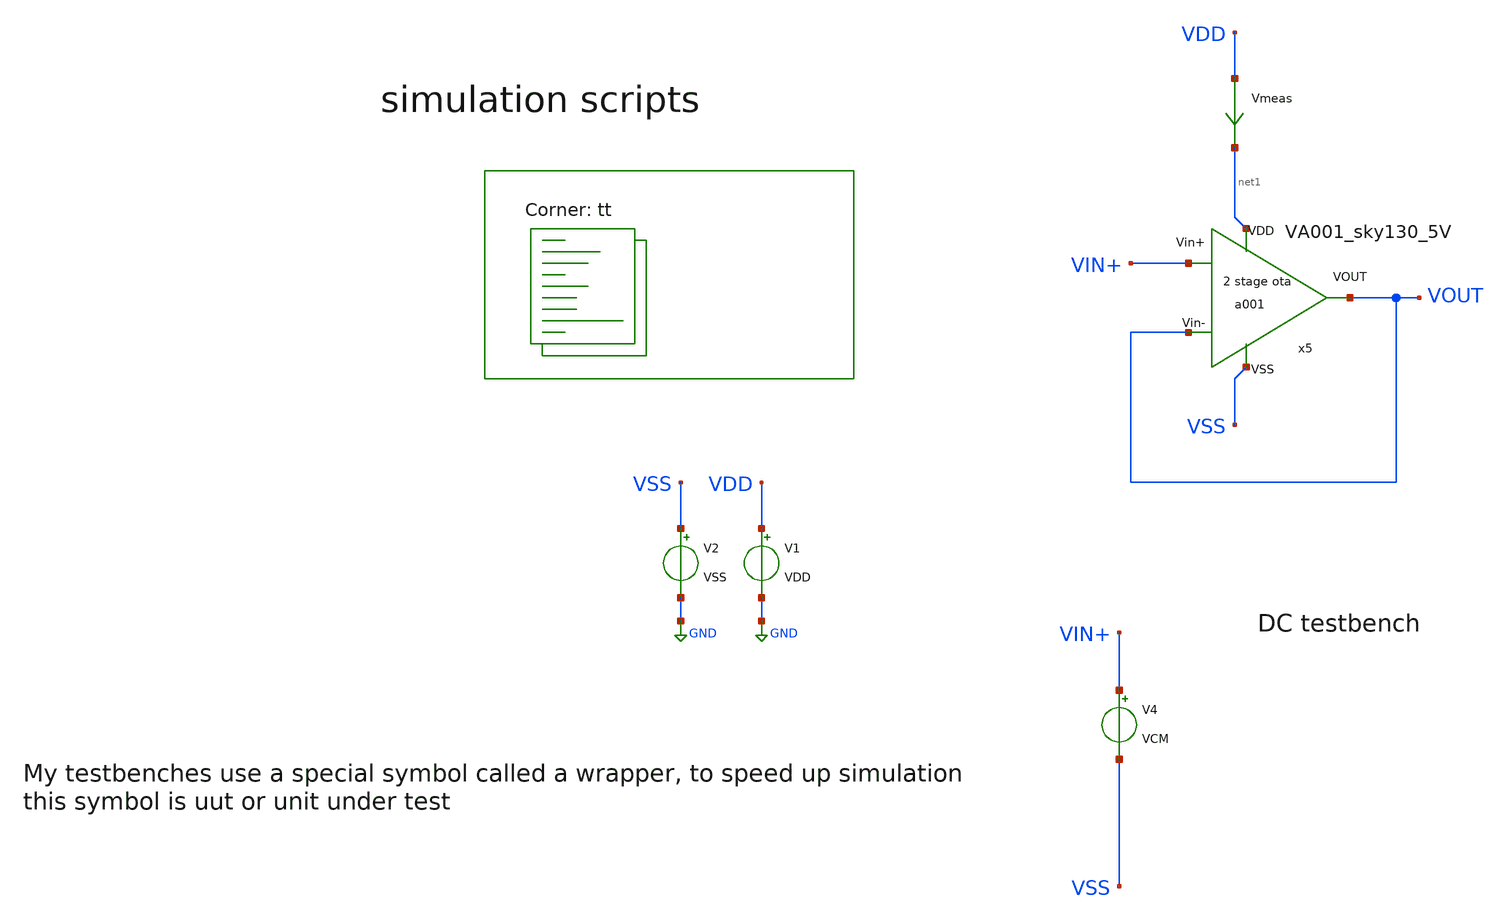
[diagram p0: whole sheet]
** sch_path: Learning/single_ended_amplifiers/Design_and_Analysis_of_Two-Stage_CMOS_Operational_Amplifier_for_Fluorescence_Signal_Processing_sky130_5V/amplifier_design/OTA_DC_TB.sch
**.subckt OTA_DC_TB
V1 VDD GND VDD
V2 VSS GND VSS
V4 VIN+ VSS VCM
Vmeas VDD net1 0
.save i(vmeas)
x5 net1 VSS VIN+ VOUT VOUT VA001_sky130_5V
**** begin user architecture code
.lib $::SKYWATER_MODELS/sky130.lib.spice tt

.Temp 27
.param VDD = 5
.param VSS = 0
.param VCM = 2.5


.control
save all
dc V4 0 5 0.01
wrdata VIN_sweep_DC.csv v(VOUT) i(Vmeas)
plot v(VOUT) v(VIN+)
plot i(Vmeas)
op
.endc


**** end user architecture code
**.ends

* expanding   symbol:  Sky130A/single ended amplifiers/VA001_sky130_5V.sym # of pins=5
** sym_path: LIB/Sky130A/single ended amplifiers/VA001_sky130_5V.sym
** sch_path: LIB/Sky130A/single ended amplifiers/VA001_sky130_5V.sch
.subckt VA001_sky130_5V VDD VSS Vin+ Vin- VOUT
*.iopin VDD
*.iopin VSS
*.iopin Vin+
*.iopin Vin-
*.iopin VOUT
XM9 VB1 VB2 net3 VSS sky130_fd_pr__nfet_g5v0d10v5 L=2 W='1 * 2 ' nf=2 ad='int((nf+1)/2) * W / nf * 0.29'
+ as='int((nf+2)/2) * W / nf * 0.29' pd='2*int((nf+1)/2) * (W / nf + 0.29)' ps='2*int((nf+2)/2) * (W / nf + 0.29)'
+ nrd='0.29 / W ' nrs='0.29 / W ' sa=0 sb=0 sd=0 mult=2 m=2
XM10 VB2 VB2 net1 VSS sky130_fd_pr__nfet_g5v0d10v5 L=2 W='1 * 2 ' nf=2 ad='int((nf+1)/2) * W / nf * 0.29'
+ as='int((nf+2)/2) * W / nf * 0.29' pd='2*int((nf+1)/2) * (W / nf + 0.29)' ps='2*int((nf+2)/2) * (W / nf + 0.29)'
+ nrd='0.29 / W ' nrs='0.29 / W ' sa=0 sb=0 sd=0 mult=2 m=2
XM3 VB2 VB1 VDD VDD sky130_fd_pr__pfet_g5v0d10v5 L=2.5 W='1 * 2 ' nf=2 ad='int((2 + 1)/2) * 1 * 0.29'
+ as='int((2 + 2)/2) * 1 * 0.29' pd='2*int((2 + 1)/2) * (1 + 0.29)' ps='2*int((2 + 2)/2) * (1 + 0.29)'
+ nrd='0.29 / 1 / 2 ' nrs='0.29 / 1 / 2 ' sa=0 sb=0 sd=0 mult=2 m=2
XM4 VB1 VB1 VDD VDD sky130_fd_pr__pfet_g5v0d10v5 L=2.5 W='1 * 2 ' nf=2 ad='int((2 + 1)/2) * 1 * 0.29'
+ as='int((2 + 2)/2) * 1 * 0.29' pd='2*int((2 + 1)/2) * (1 + 0.29)' ps='2*int((2 + 2)/2) * (1 + 0.29)'
+ nrd='0.29 / 1 / 2 ' nrs='0.29 / 1 / 2 ' sa=0 sb=0 sd=0 mult=2 m=2
XM5 net1 net1 VSS VSS sky130_fd_pr__nfet_g5v0d10v5 L=3 W='1.2 * 2 ' nf=2 ad='int((nf+1)/2) * W / nf * 0.29'
+ as='int((nf+2)/2) * W / nf * 0.29' pd='2*int((nf+1)/2) * (W / nf + 0.29)' ps='2*int((nf+2)/2) * (W / nf + 0.29)'
+ nrd='0.29 / W ' nrs='0.29 / W ' sa=0 sb=0 sd=0 mult=2 m=2
XM6 net3 net1 net2 VSS sky130_fd_pr__nfet_g5v0d10v5 L=3 W='1.2 * 2 ' nf=2 ad='int((nf+1)/2) * W / nf * 0.29'
+ as='int((nf+2)/2) * W / nf * 0.29' pd='2*int((nf+1)/2) * (W / nf + 0.29)' ps='2*int((nf+2)/2) * (W / nf + 0.29)'
+ nrd='0.29 / W ' nrs='0.29 / W ' sa=0 sb=0 sd=0 mult=8 m=8
XR2 VSS net2 VSS sky130_fd_pr__res_high_po_0p35 L=20 mult=1 m=1
XM1 net4 VB1 VDD VDD sky130_fd_pr__pfet_g5v0d10v5 L=2.5 W='1 * 2 ' nf=2 ad='int((2 + 1)/2) * 1 * 0.29'
+ as='int((2 + 2)/2) * 1 * 0.29' pd='2*int((2 + 1)/2) * (1 + 0.29)' ps='2*int((2 + 2)/2) * (1 + 0.29)'
+ nrd='0.29 / 1 / 2 ' nrs='0.29 / 1 / 2 ' sa=0 sb=0 sd=0 mult=6 m=6
XM2 net6 Vin- net4 net4 sky130_fd_pr__pfet_g5v0d10v5 L=1 W='3 * 2 ' nf=2 ad='int((2 + 1)/2) * 3 * 0.29'
+ as='int((2 + 2)/2) * 3 * 0.29' pd='2*int((2 + 1)/2) * (3 + 0.29)' ps='2*int((2 + 2)/2) * (3 + 0.29)'
+ nrd='0.29 / 3 / 2 ' nrs='0.29 / 3 / 2 ' sa=0 sb=0 sd=0 mult=4 m=4
XM11 net6 net6 VSS VSS sky130_fd_pr__nfet_g5v0d10v5 L=2 W='1.2 * 2 ' nf=2 ad='int((nf+1)/2) * W / nf * 0.29'
+ as='int((nf+2)/2) * W / nf * 0.29' pd='2*int((nf+1)/2) * (W / nf + 0.29)' ps='2*int((nf+2)/2) * (W / nf + 0.29)'
+ nrd='0.29 / W ' nrs='0.29 / W ' sa=0 sb=0 sd=0 mult=2 m=2
XM8 net5 net6 VSS VSS sky130_fd_pr__nfet_g5v0d10v5 L=2 W='1.2 * 2 ' nf=2 ad='int((nf+1)/2) * W / nf * 0.29'
+ as='int((nf+2)/2) * W / nf * 0.29' pd='2*int((nf+1)/2) * (W / nf + 0.29)' ps='2*int((nf+2)/2) * (W / nf + 0.29)'
+ nrd='0.29 / W ' nrs='0.29 / W ' sa=0 sb=0 sd=0 mult=2 m=2
XM12 VOUT net5 VSS VSS sky130_fd_pr__nfet_g5v0d10v5 L=1 W='2 * 4 ' nf=4 ad='int((nf+1)/2) * W / nf * 0.29'
+ as='int((nf+2)/2) * W / nf * 0.29' pd='2*int((nf+1)/2) * (W / nf + 0.29)' ps='2*int((nf+2)/2) * (W / nf + 0.29)'
+ nrd='0.29 / W ' nrs='0.29 / W ' sa=0 sb=0 sd=0 mult=2 m=2
XM7 net5 Vin+ net4 net4 sky130_fd_pr__pfet_g5v0d10v5 L=1 W='3 * 2 ' nf=2 ad='int((2 + 1)/2) * 3 * 0.29'
+ as='int((2 + 2)/2) * 3 * 0.29' pd='2*int((2 + 1)/2) * (3 + 0.29)' ps='2*int((2 + 2)/2) * (3 + 0.29)'
+ nrd='0.29 / 3 / 2 ' nrs='0.29 / 3 / 2 ' sa=0 sb=0 sd=0 mult=4 m=4
XM13 VOUT VB1 VDD VDD sky130_fd_pr__pfet_g5v0d10v5 L=2.5 W='1 * 2 ' nf=2 ad='int((2 + 1)/2) * 1 * 0.29'
+ as='int((2 + 2)/2) * 1 * 0.29' pd='2*int((2 + 1)/2) * (1 + 0.29)' ps='2*int((2 + 2)/2) * (1 + 0.29)'
+ nrd='0.29 / 1 / 2 ' nrs='0.29 / 1 / 2 ' sa=0 sb=0 sd=0 mult=14 m=14
XM14 net7 VB2 net5 VSS sky130_fd_pr__nfet_g5v0d10v5 L=2.1 W='1.2 * 2 ' nf=2 ad='int((nf+1)/2) * W / nf * 0.29'
+ as='int((nf+2)/2) * W / nf * 0.29' pd='2*int((nf+1)/2) * (W / nf + 0.29)' ps='2*int((nf+2)/2) * (W / nf + 0.29)'
+ nrd='0.29 / W ' nrs='0.29 / W ' sa=0 sb=0 sd=0 mult=1 m=1
XC1 net7 VOUT sky130_fd_pr__cap_mim_m3_1 W=7.5 L=7.5 MF=4 m=4
.ends

.GLOBAL GND
.end
